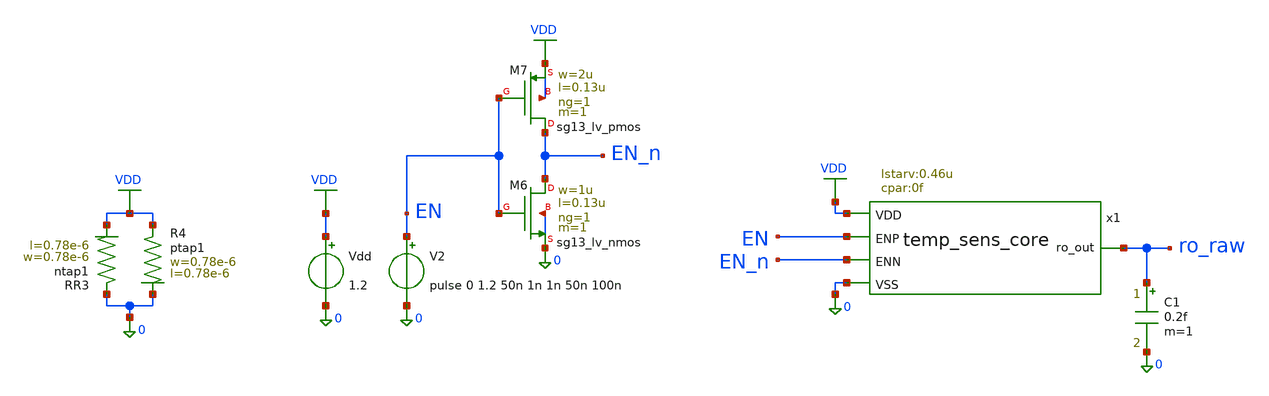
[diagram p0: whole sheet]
** sch_path: analog/temp-sens-core/testbenches/temp-sens-core_en-pv-tb.sch
**.subckt temp-sens-core_en-pv-tb
Vdd VDD 0 1.2
XR3 0 VDD ntap1 R=262.8 w=0.78e-6 l=0.78e-6
XR4 VDD 0 ptap1 R=262.8 w=0.78e-6 l=0.78e-6
XM6 EN_n EN 0 0 sg13_lv_nmos w=1u l=0.13u ng=1 m=1 mm_ok=1
XM7 EN_n EN VDD VDD sg13_lv_pmos w=2u l=0.13u ng=1 m=1 mm_ok=1
V2 EN 0 pulse 0 1.2 50n 1n 1n 50n 100n
x1 EN EN_n ro_raw VDD 0 temp_sens_core
C1 ro_raw 0 0.2f m=1
**** begin user architecture code



** ngr_lib cornerMOSlv.lib(mos_tt) mos_tt mos_ff mos_ss
** ngr_out ro_raw en en_n f

.lib cornerMOSlv.lib mos_tt
.lib cornerRES.lib res_typ

.option rshunt=1e12
.option klu
.control

tran 0.1n 1u

meas tran tperiod   TRIG v(ro_raw) VAL=0.9 RISE=2 TD=60n   TARG v(ro_raw) VAL=0.9 RISE=3 TD=60n

let f = 1/tperiod

write temp-sens-core_pvt_tt.raw time ro_raw en en_n f
.endc






** .include /foss/pdks/ihp-sg13cmos5l/libs.ref/sg13cmos5l_stdcell/spice/sg13cmos5l_stdcell.spice
.include sg13cmos5l_stdcell.spice



**** end user architecture code
**.ends

* expanding   symbol:  analog/temp-sens-core/temp_sens_core.sym # of pins=5
** sym_path: analog/temp-sens-core/temp_sens_core.sym
** sch_path: analog/temp-sens-core/temp_sens_core.sch
.subckt temp_sens_core ENP ENN ro_out VDD VSS  lstarv=0.13u cpar=0
*.opin ro_out
*.iopin VDD
*.iopin VSS
*.ipin ENP
*.ipin ENN
XM1 net1 vgp VDD VDD sg13_lv_pmos w=1.5u l={lstarv} ng=1 m=1 mm_ok=1
XM21 vgp ENP VDD VDD sg13_lv_pmos w=10u l=0.13u ng=1 m=1 mm_ok=1
XM22 vgn ENN VSS VSS sg13_lv_nmos w=10u l=0.13u ng=1 m=1 mm_ok=1
XM23 vgp vgp VDD VDD sg13_lv_pmos w=1.5u l={lstarv} ng=1 m=1 mm_ok=1
XM24 vgn vgn VSS VSS sg13_lv_nmos w=1.5u l={lstarv} ng=1 m=1 mm_ok=1
XM4 net8 vgn VSS VSS sg13_lv_nmos w=1.5u l={lstarv} ng=1 m=1 mm_ok=1
XM5 net2 vgp VDD VDD sg13_lv_pmos w=1.5u l={lstarv} ng=1 m=1 mm_ok=1
XM8 net11 vgn VSS VSS sg13_lv_nmos w=1.5u l={lstarv} ng=1 m=1 mm_ok=1
XM9 net3 vgp VDD VDD sg13_lv_pmos w=1.5u l={lstarv} ng=1 m=1 mm_ok=1
XM12 net13 vgn VSS VSS sg13_lv_nmos w=1.5u l={lstarv} ng=1 m=1 mm_ok=1
XM13 net4 vgp VDD VDD sg13_lv_pmos w=1.5u l={lstarv} ng=1 m=1 mm_ok=1
XM16 net15 vgn VSS VSS sg13_lv_nmos w=1.5u l={lstarv} ng=1 m=1 mm_ok=1
XM17 net5 vgp VDD VDD sg13_lv_pmos w=1.5u l={lstarv} ng=1 m=1 mm_ok=1
XM20 net16 vgn VSS VSS sg13_lv_nmos w=1.5u l={lstarv} ng=1 m=1 mm_ok=1
XM25 net6 vgp VDD VDD sg13_lv_pmos w=1.5u l={lstarv} ng=1 m=1 mm_ok=1
XM28 net18 vgn VSS VSS sg13_lv_nmos w=1.5u l={lstarv} ng=1 m=1 mm_ok=1
XM29 net7 vgp VDD VDD sg13_lv_pmos w=1.5u l={lstarv} ng=1 m=1 mm_ok=1
XM32 net19 vgn VSS VSS sg13_lv_nmos w=1.5u l={lstarv} ng=1 m=1 mm_ok=1
x1 net1 ro_out net9 net8 inverter
x2 net2 net9 net10 net11 inverter
x3 net3 net10 net12 net13 inverter
x4 net4 net12 net14 net15 inverter
x5 net5 net14 net22 net16 inverter
x6 net6 net22 net17 net18 inverter
x7 net7 net17 net28 net19 inverter
XM2 VSS net20 vgp VSS sg13_lv_pmos w=1u l=0.13u ng=1 m=1 mm_ok=1
XM3 VDD net21 vgn VDD sg13_lv_nmos w=1u l=0.13u ng=1 m=1 mm_ok=1
XR6 VDD net20 sub! rsil w=0.5e-6 l=75e-6 m=1 mm_ok=1
XR7 net20 VSS sub! rsil w=0.5e-6 l=10e-6 m=1 mm_ok=1
XR1 net21 VSS sub! rsil w=0.5e-6 l=75e-6 m=1 mm_ok=1
XR2 VDD net21 sub! rsil w=0.5e-6 l=10e-6 m=1 mm_ok=1
C1 net9 VSS {cpar} m=1
C2 net10 VSS {cpar} m=1
C3 net12 VSS {cpar} m=1
C4 net14 VSS {cpar} m=1
C5 net22 VSS {cpar} m=1
C6 net17 VSS {cpar} m=1
C7 net28 VSS {cpar} m=1
XM6 net23 vgp VDD VDD sg13_lv_pmos w=1.5u l={lstarv} ng=1 m=1 mm_ok=1
XM7 net26 vgn VSS VSS sg13_lv_nmos w=1.5u l={lstarv} ng=1 m=1 mm_ok=1
XM10 net24 vgp VDD VDD sg13_lv_pmos w=1.5u l={lstarv} ng=1 m=1 mm_ok=1
XM11 net27 vgn VSS VSS sg13_lv_nmos w=1.5u l={lstarv} ng=1 m=1 mm_ok=1
x8 net23 net28 net25 net26 inverter
x9 net24 net25 ro_out net27 inverter
C8 net25 VSS {cpar} m=1
C9 ro_out VSS {cpar} m=1
**** begin user architecture code



**.include /foss/pdks/ihp-sg13cmos5l/libs.ref/sg13cmos5l_stdcell/spice/sg13cmos5l_stdcell.spice
.include sg13cmos5l_stdcell.spice



**** end user architecture code
XM14 ro_out ENN VSS VSS sg13_lv_nmos w=0.5u l=0.13u ng=1 m=1 mm_ok=1
.ends


* expanding   symbol:  analog/inverter/inverter.sym # of pins=4
** sym_path: analog/inverter/inverter.sym
** sch_path: analog/inverter/inverter.sch
.subckt inverter pos in out neg
*.ipin in
*.iopin pos
*.iopin neg
*.opin out
XM1 out in neg neg sg13_lv_nmos w=2.0u l=0.45u ng=1 m=1 mm_ok=1
XM2 pos in out pos sg13_lv_pmos w=1.0u l=0.45u ng=1 m=1 mm_ok=1
.ends

.GLOBAL VDD
.end
